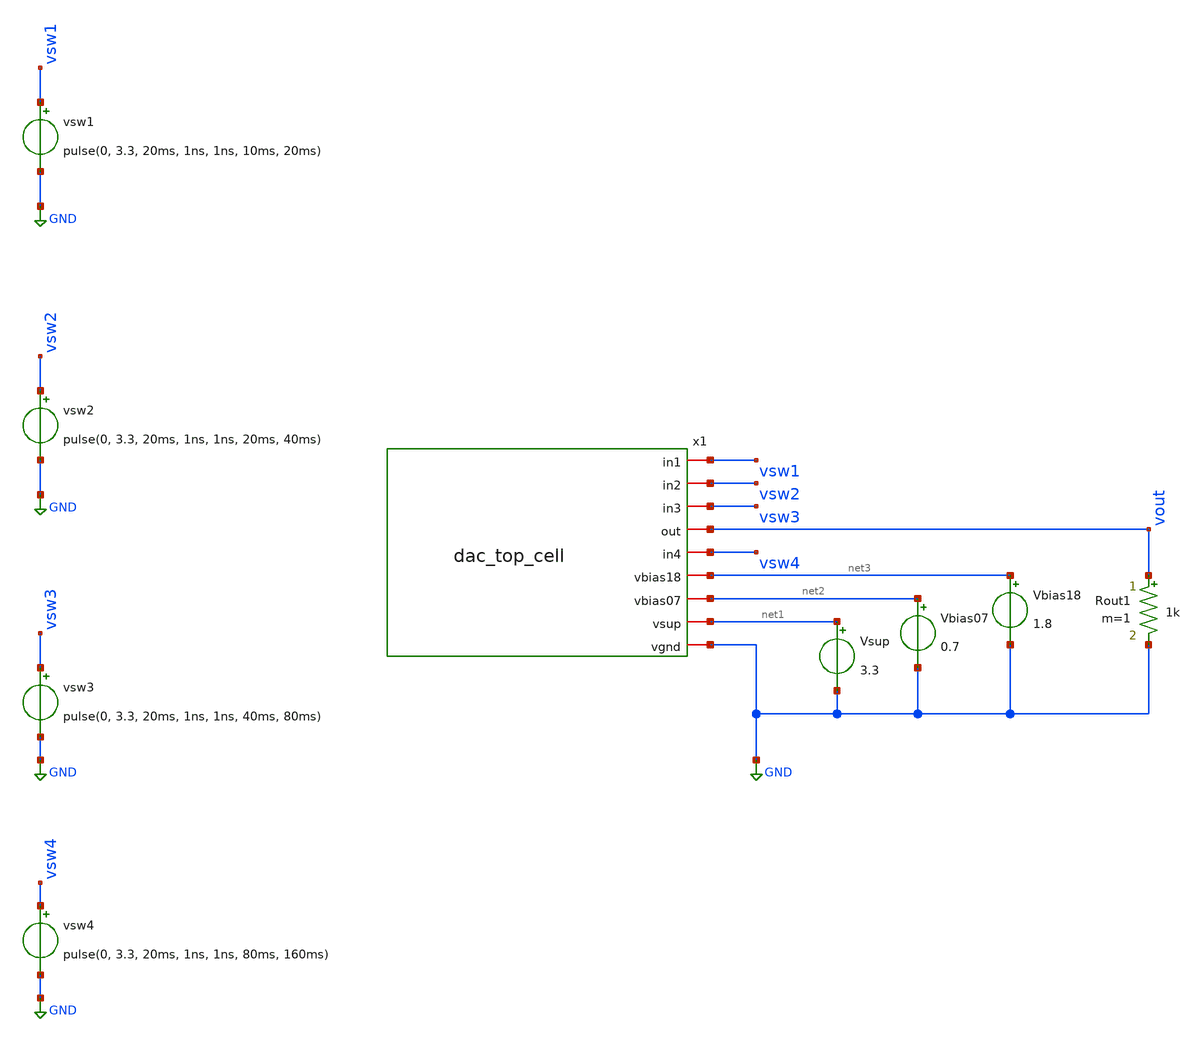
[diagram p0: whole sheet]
** sch_path: dev/top_cell_esd/tb/tb_dac_top_cell_extracted_tran.sch
**.subckt tb_dac_top_cell_extracted_tran
vsw1 vsw1 GND pulse(0, 3.3, 20ms, 1ns, 1ns, 10ms, 20ms)
vsw2 vsw2 GND pulse(0, 3.3, 20ms, 1ns, 1ns, 20ms, 40ms)
vsw3 vsw3 GND pulse(0, 3.3, 20ms, 1ns, 1ns, 40ms, 80ms)
vsw4 vsw4 GND pulse(0, 3.3, 20ms, 1ns, 1ns, 80ms, 160ms)
Rout1 vout GND 1k m=1
Vsup net1 GND 3.3
Vbias07 net2 GND 0.7
x1 vsw1 vsw2 vsw3 vout vsw4 net3 net2 net1 GND dac_top_cell
Vbias18 net3 GND 1.8
**** begin user architecture code


.lib "/usr/share/pdk/sky130A/libs.tech/ngspice/sky130.lib.spice" tt
.param mc_mm_switch=0
.param mc_pr_switch=0
*** ANALYSIS TO DO

.tran 0.1 500m 0.001m
.save vout
.save i(x1.Vo1)
.save x1.op_amp_in
.save vsw1 vsw2 vsw3 vsw4

.control
set wr_vecnames
set wr_singlescale

run
******** results filename  ************ nodes to write
wrdata $DEV_PATH/res/dac_top_cell_extracted_vout_tran_vol.res vout
wrdata $DEV_PATH/res/dac_top_cell_extracted_vsw1_tran_vol.res vsw1
wrdata $DEV_PATH/res/dac_top_cell_extracted_vsw2_tran_vol.res vsw2
wrdata $DEV_PATH/res/dac_top_cell_extracted_vsw3_tran_vol.res vsw3
wrdata $DEV_PATH/res/dac_top_cell_extracted_vsw4_tran_vol.res vsw4
.endc


**** end user architecture code
**.ends
.GLOBAL GND
.end
